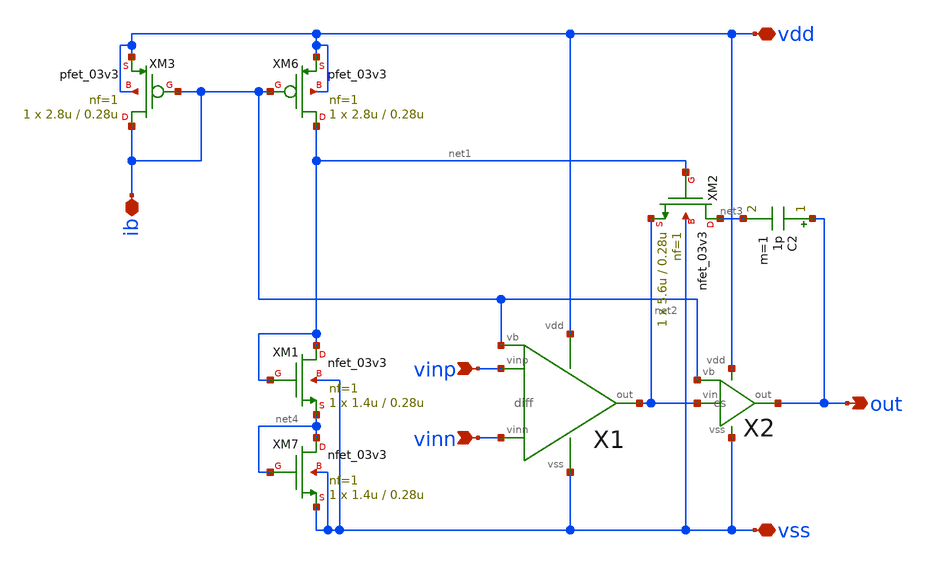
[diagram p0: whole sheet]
** sch_path: opamp/opamp.sch
**.subckt opamp vinp vinn out vdd vss ib
*.ipin vinp
*.ipin vinn
*.opin out
*.iopin vdd
*.iopin vss
*.iopin ib
X1 vinp vinn net2 vdd vss ib diff
X2 net2 ib out vdd vss cs
C2 out net3 1p m=1
XM6 net1 ib vdd vdd pfet_03v3 L=0.28u W=2.8u nf=1 ad='int((nf+1)/2) * W/nf * 0.18u' as='int((nf+2)/2) * W/nf * 0.18u'
+ pd='2*int((nf+1)/2) * (W/nf + 0.18u)' ps='2*int((nf+2)/2) * (W/nf + 0.18u)' nrd='0.18u / W' nrs='0.18u / W'
+ sa=0 sb=0 sd=0 m=1
XM7 net4 net4 vss vss nfet_03v3 L=0.28u W=1.4u nf=1 ad='int((nf+1)/2) * W/nf * 0.18u' as='int((nf+2)/2) * W/nf * 0.18u'
+ pd='2*int((nf+1)/2) * (W/nf + 0.18u)' ps='2*int((nf+2)/2) * (W/nf + 0.18u)' nrd='0.18u / W' nrs='0.18u / W'
+ sa=0 sb=0 sd=0 m=1
XM1 net1 net1 net4 vss nfet_03v3 L=0.28u W=1.4u nf=1 ad='int((nf+1)/2) * W/nf * 0.18u' as='int((nf+2)/2) * W/nf * 0.18u'
+ pd='2*int((nf+1)/2) * (W/nf + 0.18u)' ps='2*int((nf+2)/2) * (W/nf + 0.18u)' nrd='0.18u / W' nrs='0.18u / W'
+ sa=0 sb=0 sd=0 m=1
XM2 net3 net1 net2 vss nfet_03v3 L=0.28u W=5.6u nf=1 ad='int((nf+1)/2) * W/nf * 0.18u' as='int((nf+2)/2) * W/nf * 0.18u'
+ pd='2*int((nf+1)/2) * (W/nf + 0.18u)' ps='2*int((nf+2)/2) * (W/nf + 0.18u)' nrd='0.18u / W' nrs='0.18u / W'
+ sa=0 sb=0 sd=0 m=1
XM3 ib ib vdd vdd pfet_03v3 L=0.28u W=2.8u nf=1 ad='int((nf+1)/2) * W/nf * 0.18u' as='int((nf+2)/2) * W/nf * 0.18u'
+ pd='2*int((nf+1)/2) * (W/nf + 0.18u)' ps='2*int((nf+2)/2) * (W/nf + 0.18u)' nrd='0.18u / W' nrs='0.18u / W'
+ sa=0 sb=0 sd=0 m=1
**.ends
.end
